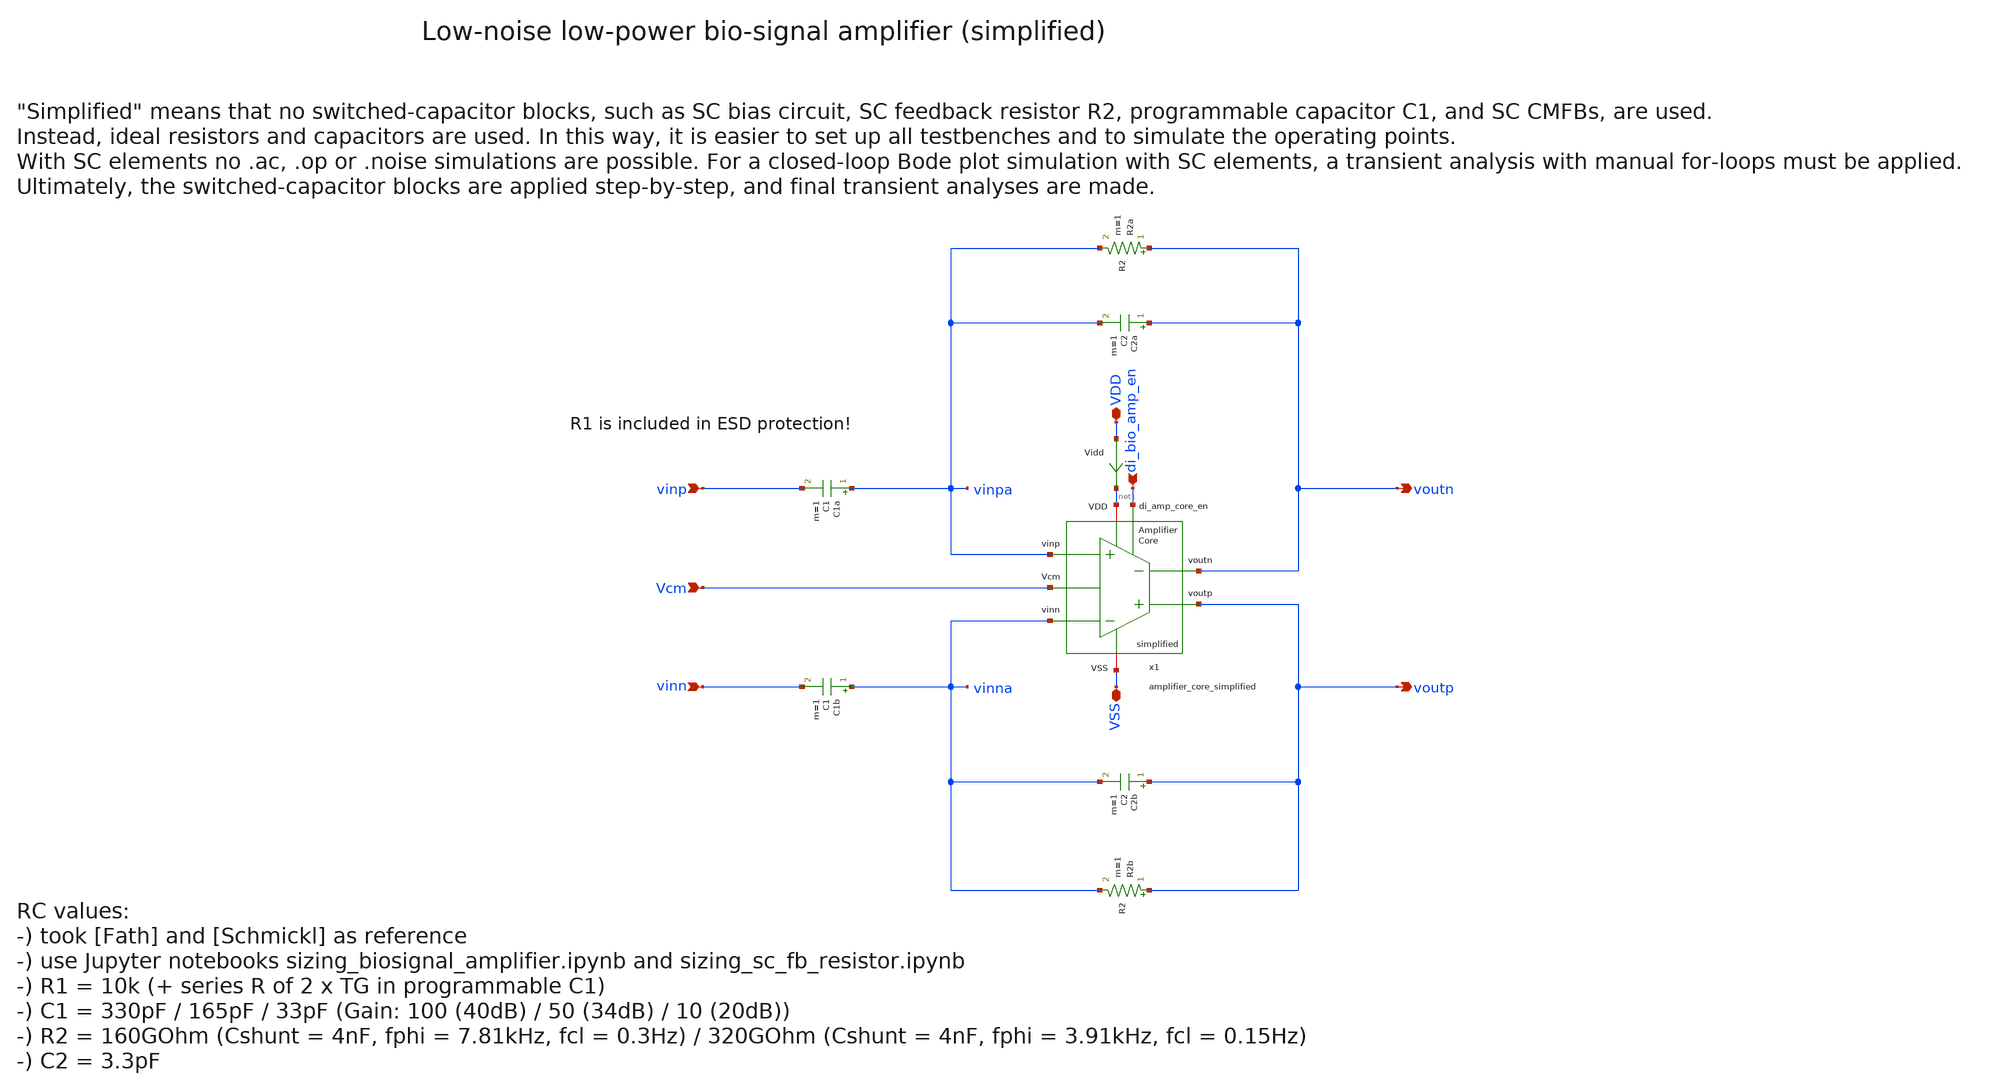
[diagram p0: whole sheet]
** sch_path: SG13G2_ATBS-ADC-main/xschem/bio_amplifier/bio_amplifier_simplified.sch
**.subckt bio_amplifier_simplified VDD VSS voutp vinp vinn voutn di_bio_amp_en Vcm
*.iopin VDD
*.iopin VSS
*.opin voutp
*.ipin vinp
*.ipin vinn
*.opin voutn
*.ipin di_bio_amp_en
*.ipin Vcm
R2a voutn vinpa R2 m=1
R2b voutp vinna R2 m=1
C2a voutn vinpa C2 m=1
C2b voutp vinna C2 m=1
C1a vinpa vinp C1 m=1
C1b vinna vinn C1 m=1
x1 voutp voutn di_bio_amp_en vinna vinpa net1 VSS Vcm amplifier_core_simplified
Vidd VDD net1 0
.save i(vidd)
**.ends
.end
